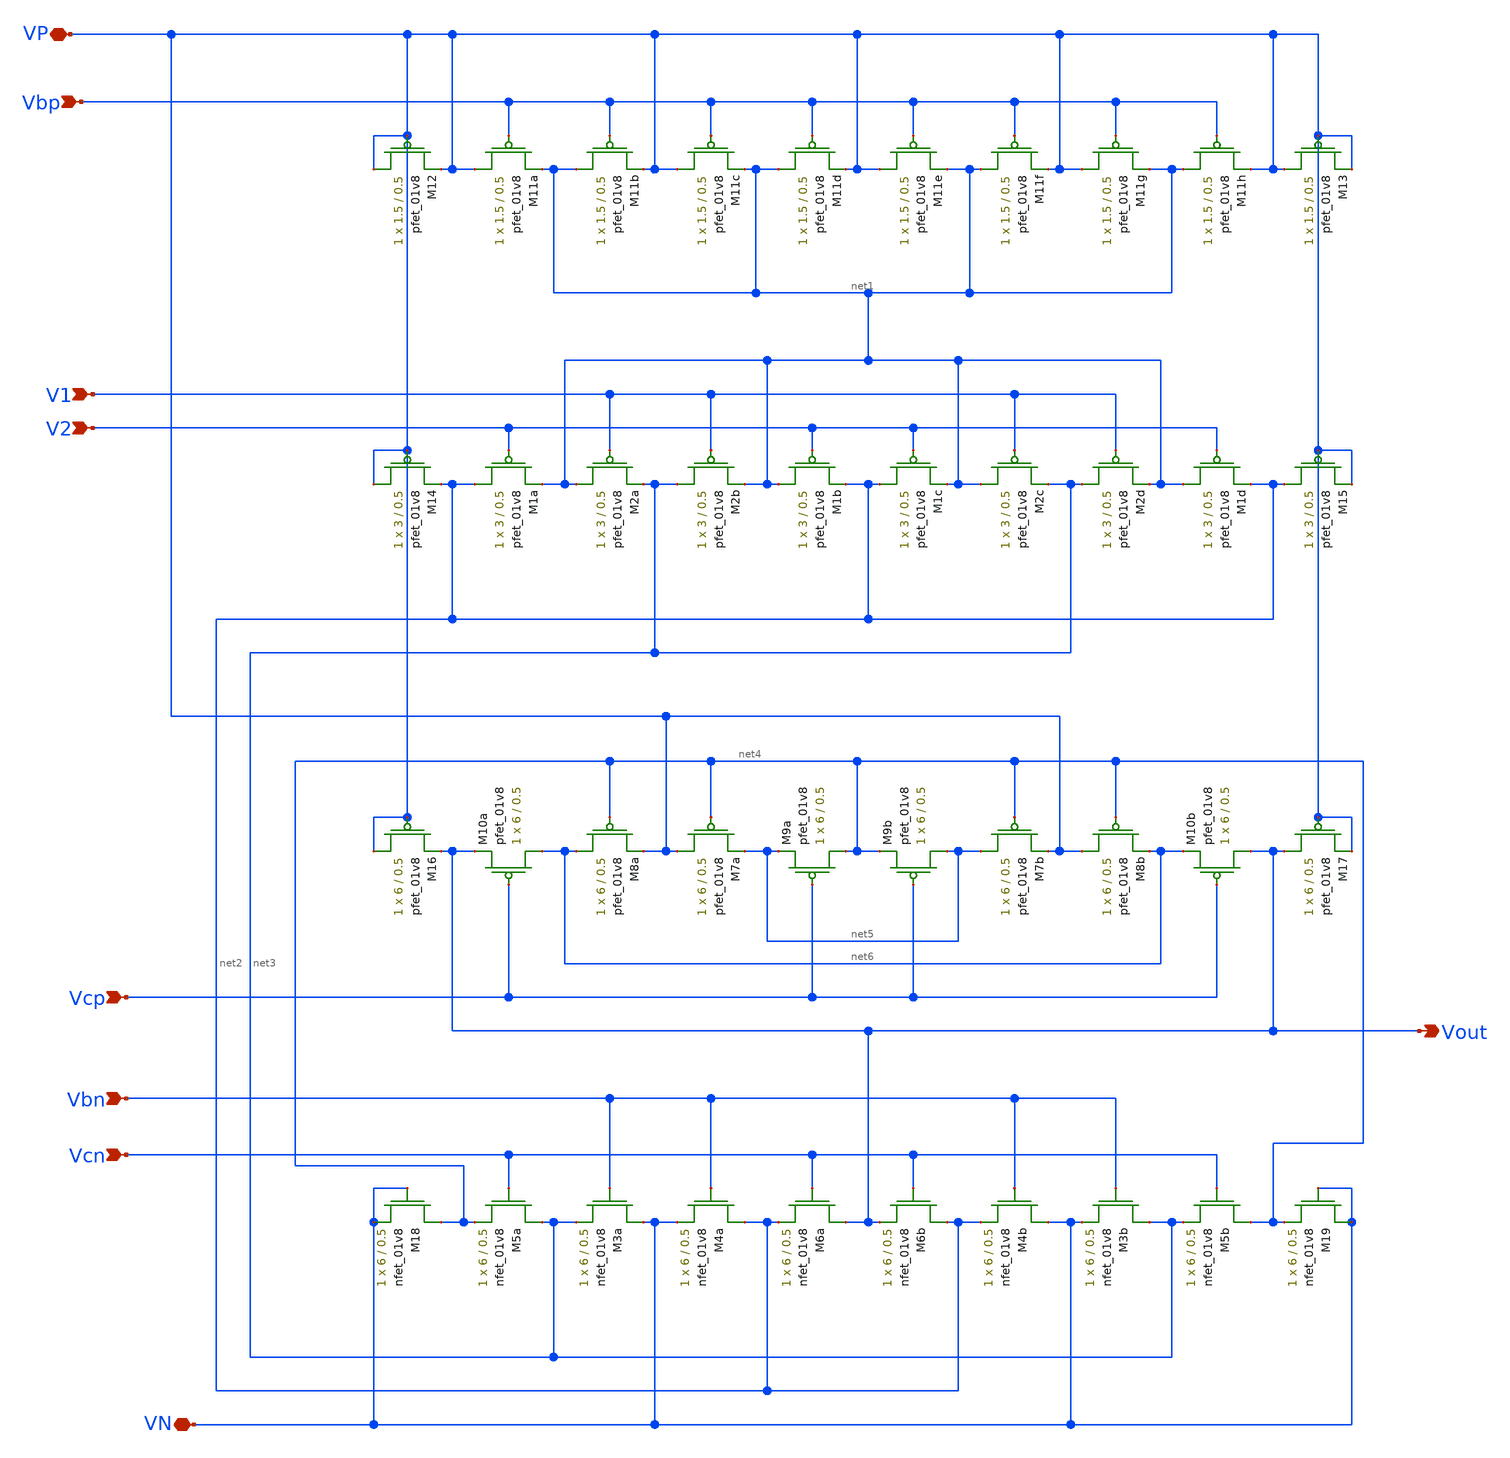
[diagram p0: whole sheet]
** sch_path: MP3/cascode-lds.sch
**.subckt cascode-lds VP VN Vbp V2 V1 Vcp Vbn Vcn Vout
*.iopin VP
*.iopin VN
*.ipin Vbp
*.ipin V2
*.ipin V1
*.ipin Vcp
*.ipin Vbn
*.ipin Vcn
*.opin Vout
XM11a VP Vbp net1 VDD sky130_fd_pr__pfet_01v8 L=0.5 W=1.5 nf=1 ad='int((nf+1)/2) * W/nf * 0.29' as='int((nf+2)/2) * W/nf * 0.29'
+ pd='2*int((nf+1)/2) * (W/nf + 0.29)' ps='2*int((nf+2)/2) * (W/nf + 0.29)' nrd='0.29 / W' nrs='0.29 / W'
+ sa=0 sb=0 sd=0 mult=1 m=1
XM11b net1 Vbp VP VDD sky130_fd_pr__pfet_01v8 L=0.5 W=1.5 nf=1 ad='int((nf+1)/2) * W/nf * 0.29' as='int((nf+2)/2) * W/nf * 0.29'
+ pd='2*int((nf+1)/2) * (W/nf + 0.29)' ps='2*int((nf+2)/2) * (W/nf + 0.29)' nrd='0.29 / W' nrs='0.29 / W'
+ sa=0 sb=0 sd=0 mult=1 m=1
XM11c VP Vbp net1 VDD sky130_fd_pr__pfet_01v8 L=0.5 W=1.5 nf=1 ad='int((nf+1)/2) * W/nf * 0.29' as='int((nf+2)/2) * W/nf * 0.29'
+ pd='2*int((nf+1)/2) * (W/nf + 0.29)' ps='2*int((nf+2)/2) * (W/nf + 0.29)' nrd='0.29 / W' nrs='0.29 / W'
+ sa=0 sb=0 sd=0 mult=1 m=1
XM11d net1 Vbp VP VDD sky130_fd_pr__pfet_01v8 L=0.5 W=1.5 nf=1 ad='int((nf+1)/2) * W/nf * 0.29' as='int((nf+2)/2) * W/nf * 0.29'
+ pd='2*int((nf+1)/2) * (W/nf + 0.29)' ps='2*int((nf+2)/2) * (W/nf + 0.29)' nrd='0.29 / W' nrs='0.29 / W'
+ sa=0 sb=0 sd=0 mult=1 m=1
XM11e VP Vbp net1 VDD sky130_fd_pr__pfet_01v8 L=0.5 W=1.5 nf=1 ad='int((nf+1)/2) * W/nf * 0.29' as='int((nf+2)/2) * W/nf * 0.29'
+ pd='2*int((nf+1)/2) * (W/nf + 0.29)' ps='2*int((nf+2)/2) * (W/nf + 0.29)' nrd='0.29 / W' nrs='0.29 / W'
+ sa=0 sb=0 sd=0 mult=1 m=1
XM11f net1 Vbp VP VDD sky130_fd_pr__pfet_01v8 L=0.5 W=1.5 nf=1 ad='int((nf+1)/2) * W/nf * 0.29' as='int((nf+2)/2) * W/nf * 0.29'
+ pd='2*int((nf+1)/2) * (W/nf + 0.29)' ps='2*int((nf+2)/2) * (W/nf + 0.29)' nrd='0.29 / W' nrs='0.29 / W'
+ sa=0 sb=0 sd=0 mult=1 m=1
XM11g VP Vbp net1 VDD sky130_fd_pr__pfet_01v8 L=0.5 W=1.5 nf=1 ad='int((nf+1)/2) * W/nf * 0.29' as='int((nf+2)/2) * W/nf * 0.29'
+ pd='2*int((nf+1)/2) * (W/nf + 0.29)' ps='2*int((nf+2)/2) * (W/nf + 0.29)' nrd='0.29 / W' nrs='0.29 / W'
+ sa=0 sb=0 sd=0 mult=1 m=1
XM11h net1 Vbp VP VDD sky130_fd_pr__pfet_01v8 L=0.5 W=1.5 nf=1 ad='int((nf+1)/2) * W/nf * 0.29' as='int((nf+2)/2) * W/nf * 0.29'
+ pd='2*int((nf+1)/2) * (W/nf + 0.29)' ps='2*int((nf+2)/2) * (W/nf + 0.29)' nrd='0.29 / W' nrs='0.29 / W'
+ sa=0 sb=0 sd=0 mult=1 m=1
XM10a net6 Vcp Vout VDD sky130_fd_pr__pfet_01v8 L=0.5 W=6 nf=1 ad='int((nf+1)/2) * W/nf * 0.29' as='int((nf+2)/2) * W/nf * 0.29'
+ pd='2*int((nf+1)/2) * (W/nf + 0.29)' ps='2*int((nf+2)/2) * (W/nf + 0.29)' nrd='0.29 / W' nrs='0.29 / W'
+ sa=0 sb=0 sd=0 mult=1 m=1
XM8a net6 net4 VP VDD sky130_fd_pr__pfet_01v8 L=0.5 W=6 nf=1 ad='int((nf+1)/2) * W/nf * 0.29' as='int((nf+2)/2) * W/nf * 0.29'
+ pd='2*int((nf+1)/2) * (W/nf + 0.29)' ps='2*int((nf+2)/2) * (W/nf + 0.29)' nrd='0.29 / W' nrs='0.29 / W'
+ sa=0 sb=0 sd=0 mult=1 m=1
XM7a VP net4 net5 VDD sky130_fd_pr__pfet_01v8 L=0.5 W=6 nf=1 ad='int((nf+1)/2) * W/nf * 0.29' as='int((nf+2)/2) * W/nf * 0.29'
+ pd='2*int((nf+1)/2) * (W/nf + 0.29)' ps='2*int((nf+2)/2) * (W/nf + 0.29)' nrd='0.29 / W' nrs='0.29 / W'
+ sa=0 sb=0 sd=0 mult=1 m=1
XM9a net4 Vcp net5 VDD sky130_fd_pr__pfet_01v8 L=0.5 W=6 nf=1 ad='int((nf+1)/2) * W/nf * 0.29' as='int((nf+2)/2) * W/nf * 0.29'
+ pd='2*int((nf+1)/2) * (W/nf + 0.29)' ps='2*int((nf+2)/2) * (W/nf + 0.29)' nrd='0.29 / W' nrs='0.29 / W'
+ sa=0 sb=0 sd=0 mult=1 m=1
XM9b net5 Vcp net4 VDD sky130_fd_pr__pfet_01v8 L=0.5 W=6 nf=1 ad='int((nf+1)/2) * W/nf * 0.29' as='int((nf+2)/2) * W/nf * 0.29'
+ pd='2*int((nf+1)/2) * (W/nf + 0.29)' ps='2*int((nf+2)/2) * (W/nf + 0.29)' nrd='0.29 / W' nrs='0.29 / W'
+ sa=0 sb=0 sd=0 mult=1 m=1
XM7b net5 net4 VP VDD sky130_fd_pr__pfet_01v8 L=0.5 W=6 nf=1 ad='int((nf+1)/2) * W/nf * 0.29' as='int((nf+2)/2) * W/nf * 0.29'
+ pd='2*int((nf+1)/2) * (W/nf + 0.29)' ps='2*int((nf+2)/2) * (W/nf + 0.29)' nrd='0.29 / W' nrs='0.29 / W'
+ sa=0 sb=0 sd=0 mult=1 m=1
XM8b VP net4 net6 VDD sky130_fd_pr__pfet_01v8 L=0.5 W=6 nf=1 ad='int((nf+1)/2) * W/nf * 0.29' as='int((nf+2)/2) * W/nf * 0.29'
+ pd='2*int((nf+1)/2) * (W/nf + 0.29)' ps='2*int((nf+2)/2) * (W/nf + 0.29)' nrd='0.29 / W' nrs='0.29 / W'
+ sa=0 sb=0 sd=0 mult=1 m=1
XM10b Vout Vcp net6 VDD sky130_fd_pr__pfet_01v8 L=0.5 W=6 nf=1 ad='int((nf+1)/2) * W/nf * 0.29' as='int((nf+2)/2) * W/nf * 0.29'
+ pd='2*int((nf+1)/2) * (W/nf + 0.29)' ps='2*int((nf+2)/2) * (W/nf + 0.29)' nrd='0.29 / W' nrs='0.29 / W'
+ sa=0 sb=0 sd=0 mult=1 m=1
XM1a net2 V2 net1 VDD sky130_fd_pr__pfet_01v8 L=0.5 W=3 nf=1 ad='int((nf+1)/2) * W/nf * 0.29' as='int((nf+2)/2) * W/nf * 0.29'
+ pd='2*int((nf+1)/2) * (W/nf + 0.29)' ps='2*int((nf+2)/2) * (W/nf + 0.29)' nrd='0.29 / W' nrs='0.29 / W'
+ sa=0 sb=0 sd=0 mult=1 m=1
XM2a net1 V1 net3 VDD sky130_fd_pr__pfet_01v8 L=0.5 W=3 nf=1 ad='int((nf+1)/2) * W/nf * 0.29' as='int((nf+2)/2) * W/nf * 0.29'
+ pd='2*int((nf+1)/2) * (W/nf + 0.29)' ps='2*int((nf+2)/2) * (W/nf + 0.29)' nrd='0.29 / W' nrs='0.29 / W'
+ sa=0 sb=0 sd=0 mult=1 m=1
XM2b net3 V1 net1 VDD sky130_fd_pr__pfet_01v8 L=0.5 W=3 nf=1 ad='int((nf+1)/2) * W/nf * 0.29' as='int((nf+2)/2) * W/nf * 0.29'
+ pd='2*int((nf+1)/2) * (W/nf + 0.29)' ps='2*int((nf+2)/2) * (W/nf + 0.29)' nrd='0.29 / W' nrs='0.29 / W'
+ sa=0 sb=0 sd=0 mult=1 m=1
XM1b net1 V2 net2 VDD sky130_fd_pr__pfet_01v8 L=0.5 W=3 nf=1 ad='int((nf+1)/2) * W/nf * 0.29' as='int((nf+2)/2) * W/nf * 0.29'
+ pd='2*int((nf+1)/2) * (W/nf + 0.29)' ps='2*int((nf+2)/2) * (W/nf + 0.29)' nrd='0.29 / W' nrs='0.29 / W'
+ sa=0 sb=0 sd=0 mult=1 m=1
XM1c net2 V2 net1 VDD sky130_fd_pr__pfet_01v8 L=0.5 W=3 nf=1 ad='int((nf+1)/2) * W/nf * 0.29' as='int((nf+2)/2) * W/nf * 0.29'
+ pd='2*int((nf+1)/2) * (W/nf + 0.29)' ps='2*int((nf+2)/2) * (W/nf + 0.29)' nrd='0.29 / W' nrs='0.29 / W'
+ sa=0 sb=0 sd=0 mult=1 m=1
XM2c net1 V1 net3 VDD sky130_fd_pr__pfet_01v8 L=0.5 W=3 nf=1 ad='int((nf+1)/2) * W/nf * 0.29' as='int((nf+2)/2) * W/nf * 0.29'
+ pd='2*int((nf+1)/2) * (W/nf + 0.29)' ps='2*int((nf+2)/2) * (W/nf + 0.29)' nrd='0.29 / W' nrs='0.29 / W'
+ sa=0 sb=0 sd=0 mult=1 m=1
XM2d net3 V1 net1 VDD sky130_fd_pr__pfet_01v8 L=0.5 W=3 nf=1 ad='int((nf+1)/2) * W/nf * 0.29' as='int((nf+2)/2) * W/nf * 0.29'
+ pd='2*int((nf+1)/2) * (W/nf + 0.29)' ps='2*int((nf+2)/2) * (W/nf + 0.29)' nrd='0.29 / W' nrs='0.29 / W'
+ sa=0 sb=0 sd=0 mult=1 m=1
XM1d net1 V2 net2 VDD sky130_fd_pr__pfet_01v8 L=0.5 W=3 nf=1 ad='int((nf+1)/2) * W/nf * 0.29' as='int((nf+2)/2) * W/nf * 0.29'
+ pd='2*int((nf+1)/2) * (W/nf + 0.29)' ps='2*int((nf+2)/2) * (W/nf + 0.29)' nrd='0.29 / W' nrs='0.29 / W'
+ sa=0 sb=0 sd=0 mult=1 m=1
XM3a VN Vbn net3 GND sky130_fd_pr__nfet_01v8 L=0.5 W=6 nf=1 ad='int((nf+1)/2) * W/nf * 0.29' as='int((nf+2)/2) * W/nf * 0.29'
+ pd='2*int((nf+1)/2) * (W/nf + 0.29)' ps='2*int((nf+2)/2) * (W/nf + 0.29)' nrd='0.29 / W' nrs='0.29 / W'
+ sa=0 sb=0 sd=0 mult=1 m=1
XM4a net2 Vbn VN GND sky130_fd_pr__nfet_01v8 L=0.5 W=6 nf=1 ad='int((nf+1)/2) * W/nf * 0.29' as='int((nf+2)/2) * W/nf * 0.29'
+ pd='2*int((nf+1)/2) * (W/nf + 0.29)' ps='2*int((nf+2)/2) * (W/nf + 0.29)' nrd='0.29 / W' nrs='0.29 / W'
+ sa=0 sb=0 sd=0 mult=1 m=1
XM6a Vout Vcn net2 GND sky130_fd_pr__nfet_01v8 L=0.5 W=6 nf=1 ad='int((nf+1)/2) * W/nf * 0.29' as='int((nf+2)/2) * W/nf * 0.29'
+ pd='2*int((nf+1)/2) * (W/nf + 0.29)' ps='2*int((nf+2)/2) * (W/nf + 0.29)' nrd='0.29 / W' nrs='0.29 / W'
+ sa=0 sb=0 sd=0 mult=1 m=1
XM6b net2 Vcn Vout GND sky130_fd_pr__nfet_01v8 L=0.5 W=6 nf=1 ad='int((nf+1)/2) * W/nf * 0.29' as='int((nf+2)/2) * W/nf * 0.29'
+ pd='2*int((nf+1)/2) * (W/nf + 0.29)' ps='2*int((nf+2)/2) * (W/nf + 0.29)' nrd='0.29 / W' nrs='0.29 / W'
+ sa=0 sb=0 sd=0 mult=1 m=1
XM4b VN Vbn net2 GND sky130_fd_pr__nfet_01v8 L=0.5 W=6 nf=1 ad='int((nf+1)/2) * W/nf * 0.29' as='int((nf+2)/2) * W/nf * 0.29'
+ pd='2*int((nf+1)/2) * (W/nf + 0.29)' ps='2*int((nf+2)/2) * (W/nf + 0.29)' nrd='0.29 / W' nrs='0.29 / W'
+ sa=0 sb=0 sd=0 mult=1 m=1
XM3b net3 Vbn VN GND sky130_fd_pr__nfet_01v8 L=0.5 W=6 nf=1 ad='int((nf+1)/2) * W/nf * 0.29' as='int((nf+2)/2) * W/nf * 0.29'
+ pd='2*int((nf+1)/2) * (W/nf + 0.29)' ps='2*int((nf+2)/2) * (W/nf + 0.29)' nrd='0.29 / W' nrs='0.29 / W'
+ sa=0 sb=0 sd=0 mult=1 m=1
XM5b net4 Vcn net3 GND sky130_fd_pr__nfet_01v8 L=0.5 W=6 nf=1 ad='int((nf+1)/2) * W/nf * 0.29' as='int((nf+2)/2) * W/nf * 0.29'
+ pd='2*int((nf+1)/2) * (W/nf + 0.29)' ps='2*int((nf+2)/2) * (W/nf + 0.29)' nrd='0.29 / W' nrs='0.29 / W'
+ sa=0 sb=0 sd=0 mult=1 m=1
XM13 VP VP VP VDD sky130_fd_pr__pfet_01v8 L=0.5 W=1.5 nf=1 ad='int((nf+1)/2) * W/nf * 0.29' as='int((nf+2)/2) * W/nf * 0.29'
+ pd='2*int((nf+1)/2) * (W/nf + 0.29)' ps='2*int((nf+2)/2) * (W/nf + 0.29)' nrd='0.29 / W' nrs='0.29 / W'
+ sa=0 sb=0 sd=0 mult=1 m=1
XM15 net2 VP VP VDD sky130_fd_pr__pfet_01v8 L=0.5 W=3 nf=1 ad='int((nf+1)/2) * W/nf * 0.29' as='int((nf+2)/2) * W/nf * 0.29'
+ pd='2*int((nf+1)/2) * (W/nf + 0.29)' ps='2*int((nf+2)/2) * (W/nf + 0.29)' nrd='0.29 / W' nrs='0.29 / W'
+ sa=0 sb=0 sd=0 mult=1 m=1
XM17 Vout VP VP VDD sky130_fd_pr__pfet_01v8 L=0.5 W=6 nf=1 ad='int((nf+1)/2) * W/nf * 0.29' as='int((nf+2)/2) * W/nf * 0.29'
+ pd='2*int((nf+1)/2) * (W/nf + 0.29)' ps='2*int((nf+2)/2) * (W/nf + 0.29)' nrd='0.29 / W' nrs='0.29 / W'
+ sa=0 sb=0 sd=0 mult=1 m=1
XM19 VN VN net4 GND sky130_fd_pr__nfet_01v8 L=0.5 W=6 nf=1 ad='int((nf+1)/2) * W/nf * 0.29' as='int((nf+2)/2) * W/nf * 0.29'
+ pd='2*int((nf+1)/2) * (W/nf + 0.29)' ps='2*int((nf+2)/2) * (W/nf + 0.29)' nrd='0.29 / W' nrs='0.29 / W'
+ sa=0 sb=0 sd=0 mult=1 m=1
XM12 VP VP VP VDD sky130_fd_pr__pfet_01v8 L=0.5 W=1.5 nf=1 ad='int((nf+1)/2) * W/nf * 0.29' as='int((nf+2)/2) * W/nf * 0.29'
+ pd='2*int((nf+1)/2) * (W/nf + 0.29)' ps='2*int((nf+2)/2) * (W/nf + 0.29)' nrd='0.29 / W' nrs='0.29 / W'
+ sa=0 sb=0 sd=0 mult=1 m=1
XM14 VP VP net2 VDD sky130_fd_pr__pfet_01v8 L=0.5 W=3 nf=1 ad='int((nf+1)/2) * W/nf * 0.29' as='int((nf+2)/2) * W/nf * 0.29'
+ pd='2*int((nf+1)/2) * (W/nf + 0.29)' ps='2*int((nf+2)/2) * (W/nf + 0.29)' nrd='0.29 / W' nrs='0.29 / W'
+ sa=0 sb=0 sd=0 mult=1 m=1
XM16 VP VP Vout VDD sky130_fd_pr__pfet_01v8 L=0.5 W=6 nf=1 ad='int((nf+1)/2) * W/nf * 0.29' as='int((nf+2)/2) * W/nf * 0.29'
+ pd='2*int((nf+1)/2) * (W/nf + 0.29)' ps='2*int((nf+2)/2) * (W/nf + 0.29)' nrd='0.29 / W' nrs='0.29 / W'
+ sa=0 sb=0 sd=0 mult=1 m=1
XM5a net3 Vcn net4 GND sky130_fd_pr__nfet_01v8 L=0.5 W=6 nf=1 ad='int((nf+1)/2) * W/nf * 0.29' as='int((nf+2)/2) * W/nf * 0.29'
+ pd='2*int((nf+1)/2) * (W/nf + 0.29)' ps='2*int((nf+2)/2) * (W/nf + 0.29)' nrd='0.29 / W' nrs='0.29 / W'
+ sa=0 sb=0 sd=0 mult=1 m=1
XM18 net4 VN VN GND sky130_fd_pr__nfet_01v8 L=0.5 W=6 nf=1 ad='int((nf+1)/2) * W/nf * 0.29' as='int((nf+2)/2) * W/nf * 0.29'
+ pd='2*int((nf+1)/2) * (W/nf + 0.29)' ps='2*int((nf+2)/2) * (W/nf + 0.29)' nrd='0.29 / W' nrs='0.29 / W'
+ sa=0 sb=0 sd=0 mult=1 m=1
**.ends
.end
